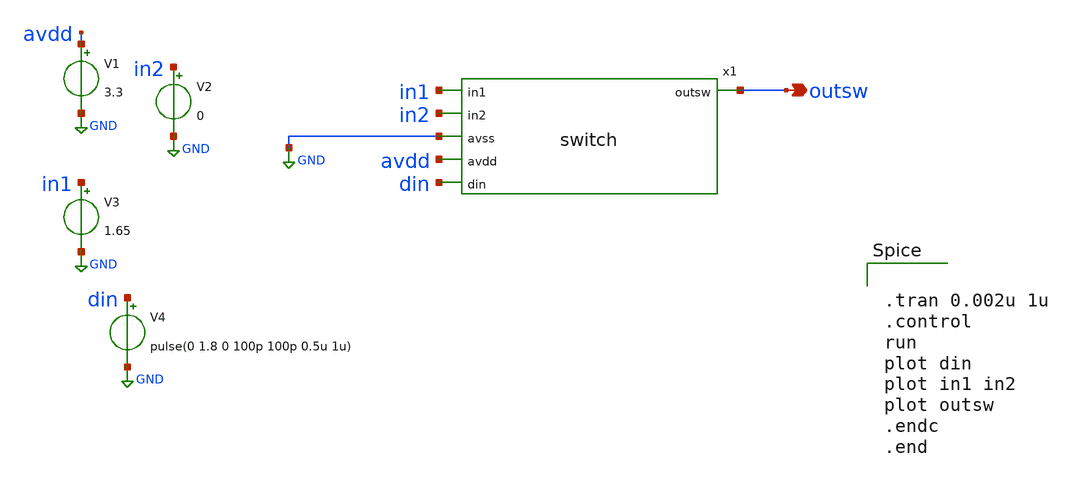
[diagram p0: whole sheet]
** sch_path: xschem/tb_switch.sch
**.subckt tb_switch outsw
*.opin outsw
V1 avdd GND 3.3
V2 in2 GND 0
V3 in1 GND 1.65
V4 din GND pulse(0 1.8 0 100p 100p 0.5u 1u)
x1 outsw in1 in2 GND avdd din switch
**** begin user architecture code

** opencircuitdesign pdks install
.lib $::SKYWATER_MODELS/sky130.lib.spice tt




.tran 0.002u 1u
.control
run
plot din
plot in1 in2
plot outsw
.endc
.end

**** end user architecture code
**.ends

* expanding   symbol:  switch.sym # of pins=6
** sym_path: xschem/switch.sym
** sch_path: xschem/switch.sch
.subckt switch outsw in1 in2 avss avdd din
*.ipin avss
*.ipin avdd
*.ipin din
*.ipin in1
*.ipin in2
*.opin outsw
XM10 dinbar din avdd avdd sky130_fd_pr__pfet_g5v0d10v5 L=0.5 W=1 nf=1 ad='int((1 + 1)/2) * 1 / 1 * 0.29'
+ as='int((1 + 2)/2) * 1 / 1 * 0.29' pd='2*int((1 + 1)/2) * (1 / 1 + 0.29)' ps='2*int((1 + 2)/2) * (1 / 1 + 0.29)'
+ nrd='0.29 / 1 ' nrs='0.29 / 1 ' sa=0 sb=0 sd=0 mult=1 m=1
XM2 dinbar din avss avss sky130_fd_pr__nfet_g5v0d10v5 L=0.5 W=1 nf=1 ad='int((1 + 1)/2) * 1 / 1 * 0.29'
+ as='int((1 + 2)/2) * 1 / 1 * 0.29' pd='2*int((1 + 1)/2) * (1 / 1 + 0.29)' ps='2*int((1 + 2)/2) * (1 / 1 + 0.29)'
+ nrd='0.29 / 1 ' nrs='0.29 / 1 ' sa=0 sb=0 sd=0 mult=1 m=1
XM1 wc dinbar avdd avdd sky130_fd_pr__pfet_g5v0d10v5 L=0.5 W=1 nf=1 ad='int((1 + 1)/2) * 1 / 1 * 0.29'
+ as='int((1 + 2)/2) * 1 / 1 * 0.29' pd='2*int((1 + 1)/2) * (1 / 1 + 0.29)' ps='2*int((1 + 2)/2) * (1 / 1 + 0.29)'
+ nrd='0.29 / 1 ' nrs='0.29 / 1 ' sa=0 sb=0 sd=0 mult=1 m=1
XM3 wc dinbar avss avss sky130_fd_pr__nfet_g5v0d10v5 L=0.5 W=1 nf=1 ad='int((1 + 1)/2) * 1 / 1 * 0.29'
+ as='int((1 + 2)/2) * 1 / 1 * 0.29' pd='2*int((1 + 1)/2) * (1 / 1 + 0.29)' ps='2*int((1 + 2)/2) * (1 / 1 + 0.29)'
+ nrd='0.29 / 1 ' nrs='0.29 / 1 ' sa=0 sb=0 sd=0 mult=1 m=1
XM5 outsw dinbar in2 avss sky130_fd_pr__nfet_g5v0d10v5 L=0.5 W=1 nf=1 ad='int((1 + 1)/2) * 1 / 1 * 0.29'
+ as='int((1 + 2)/2) * 1 / 1 * 0.29' pd='2*int((1 + 1)/2) * (1 / 1 + 0.29)' ps='2*int((1 + 2)/2) * (1 / 1 + 0.29)'
+ nrd='0.29 / 1 ' nrs='0.29 / 1 ' sa=0 sb=0 sd=0 mult=1 m=1
XM4 outsw dinbar in1 avdd sky130_fd_pr__pfet_g5v0d10v5 L=0.5 W=1 nf=1 ad='int((1 + 1)/2) * 1 / 1 * 0.29'
+ as='int((1 + 2)/2) * 1 / 1 * 0.29' pd='2*int((1 + 1)/2) * (1 / 1 + 0.29)' ps='2*int((1 + 2)/2) * (1 / 1 + 0.29)'
+ nrd='0.29 / 1 ' nrs='0.29 / 1 ' sa=0 sb=0 sd=0 mult=1 m=1
XM11 in2 wc outsw avdd sky130_fd_pr__pfet_g5v0d10v5 L=0.5 W=1 nf=1 ad='int((1 + 1)/2) * 1 / 1 * 0.29'
+ as='int((1 + 2)/2) * 1 / 1 * 0.29' pd='2*int((1 + 1)/2) * (1 / 1 + 0.29)' ps='2*int((1 + 2)/2) * (1 / 1 + 0.29)'
+ nrd='0.29 / 1 ' nrs='0.29 / 1 ' sa=0 sb=0 sd=0 mult=1 m=1
XM12 in1 wc outsw avss sky130_fd_pr__nfet_g5v0d10v5 L=0.5 W=1 nf=1 ad='int((1 + 1)/2) * 1 / 1 * 0.29'
+ as='int((1 + 2)/2) * 1 / 1 * 0.29' pd='2*int((1 + 1)/2) * (1 / 1 + 0.29)' ps='2*int((1 + 2)/2) * (1 / 1 + 0.29)'
+ nrd='0.29 / 1 ' nrs='0.29 / 1 ' sa=0 sb=0 sd=0 mult=1 m=1
.ends

.GLOBAL GND
.end
